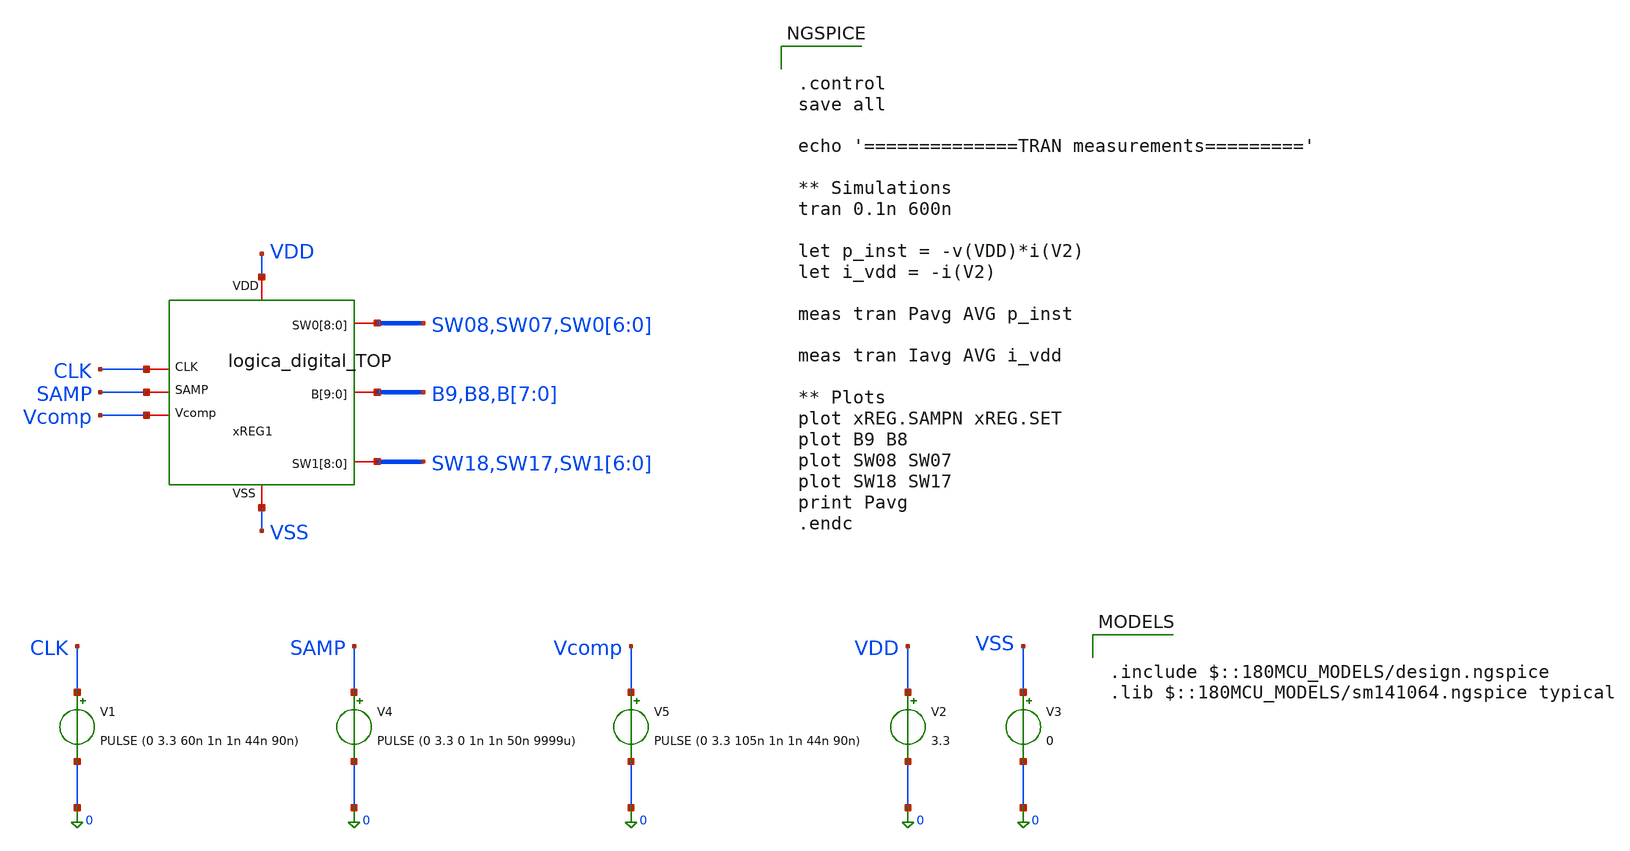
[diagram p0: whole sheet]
** sch_path: designs/sar_adc/digital/logica_digital_TOP/xschem/logica_digital_TOP_tb.sch
**.subckt logica_digital_TOP_tb
V1 CLK 0 PULSE (0 3.3 60n 1n 1n 44n 90n)
V2 VDD 0 3.3
V3 VSS 0 0
V5 Vcomp 0 PULSE (0 3.3 105n 1n 1n 44n 90n)
V4 SAMP 0 PULSE (0 3.3 0 1n 1n 50n 9999u)
xREG1 VDD CLK SAMP Vcomp SW08 SW07 SW0[6] SW0[5] SW0[4] SW0[3] SW0[2] SW0[1] SW0[0] B9 B8 B[7] B[6]
+ B[5] B[4] B[3] B[2] B[1] B[0] SW18 SW17 SW1[6] SW1[5] SW1[4] SW1[3] SW1[2] SW1[1] SW1[0] VSS
+ logica_digital_TOP
**** begin user architecture code


.control
save all

echo '==============TRAN measurements========='

** Simulations
tran 0.1n 600n

let p_inst = -v(VDD)*i(V2)
let i_vdd = -i(V2)

meas tran Pavg AVG p_inst

meas tran Iavg AVG i_vdd

** Plots
plot xREG.SAMPN xREG.SET
plot B9 B8
plot SW08 SW07
plot SW18 SW17
print Pavg
.endc



.include $::180MCU_MODELS/design.ngspice
.lib $::180MCU_MODELS/sm141064.ngspice typical

**** end user architecture code
**.ends
.end
